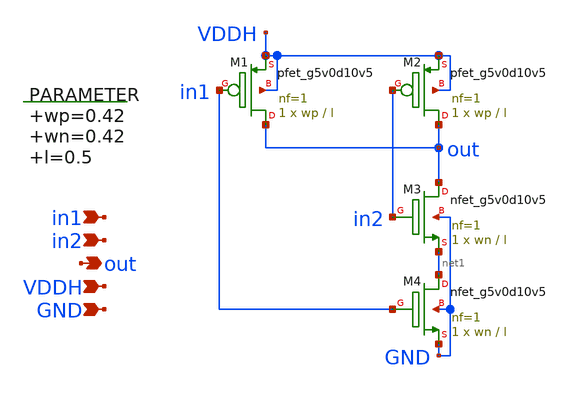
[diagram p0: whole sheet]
** sch_path: xschem/nand_hvl.sch
**.subckt nand_hvl in2 out VDDH GND in1
*.ipin in2
*.opin out
*.ipin VDDH
*.ipin GND
*.ipin in1
.param wp=0.42 wn=0.42 l=0.5
XM1 out in1 VDDH VDDH sky130_fd_pr__pfet_g5v0d10v5 L=l W=wp nf=1 ad='int((nf+1)/2) * W/nf * 0.29' as='int((nf+2)/2) * W/nf * 0.29'
+ pd='2*int((nf+1)/2) * (W/nf + 0.29)' ps='2*int((nf+2)/2) * (W/nf + 0.29)' nrd='0.29 / W' nrs='0.29 / W'
+ sa=0 sb=0 sd=0 mult=1 m=1
XM2 out in2 VDDH VDDH sky130_fd_pr__pfet_g5v0d10v5 L=l W=wp nf=1 ad='int((nf+1)/2) * W/nf * 0.29' as='int((nf+2)/2) * W/nf * 0.29'
+ pd='2*int((nf+1)/2) * (W/nf + 0.29)' ps='2*int((nf+2)/2) * (W/nf + 0.29)' nrd='0.29 / W' nrs='0.29 / W'
+ sa=0 sb=0 sd=0 mult=1 m=1
XM3 out in2 net1 GND sky130_fd_pr__nfet_g5v0d10v5 L=l W=wn nf=1 ad='int((nf+1)/2) * W/nf * 0.29' as='int((nf+2)/2) * W/nf * 0.29'
+ pd='2*int((nf+1)/2) * (W/nf + 0.29)' ps='2*int((nf+2)/2) * (W/nf + 0.29)' nrd='0.29 / W' nrs='0.29 / W'
+ sa=0 sb=0 sd=0 mult=1 m=1
XM4 net1 in1 GND GND sky130_fd_pr__nfet_g5v0d10v5 L=l W=wn nf=1 ad='int((nf+1)/2) * W/nf * 0.29' as='int((nf+2)/2) * W/nf * 0.29'
+ pd='2*int((nf+1)/2) * (W/nf + 0.29)' ps='2*int((nf+2)/2) * (W/nf + 0.29)' nrd='0.29 / W' nrs='0.29 / W'
+ sa=0 sb=0 sd=0 mult=1 m=1
**.ends
.end
